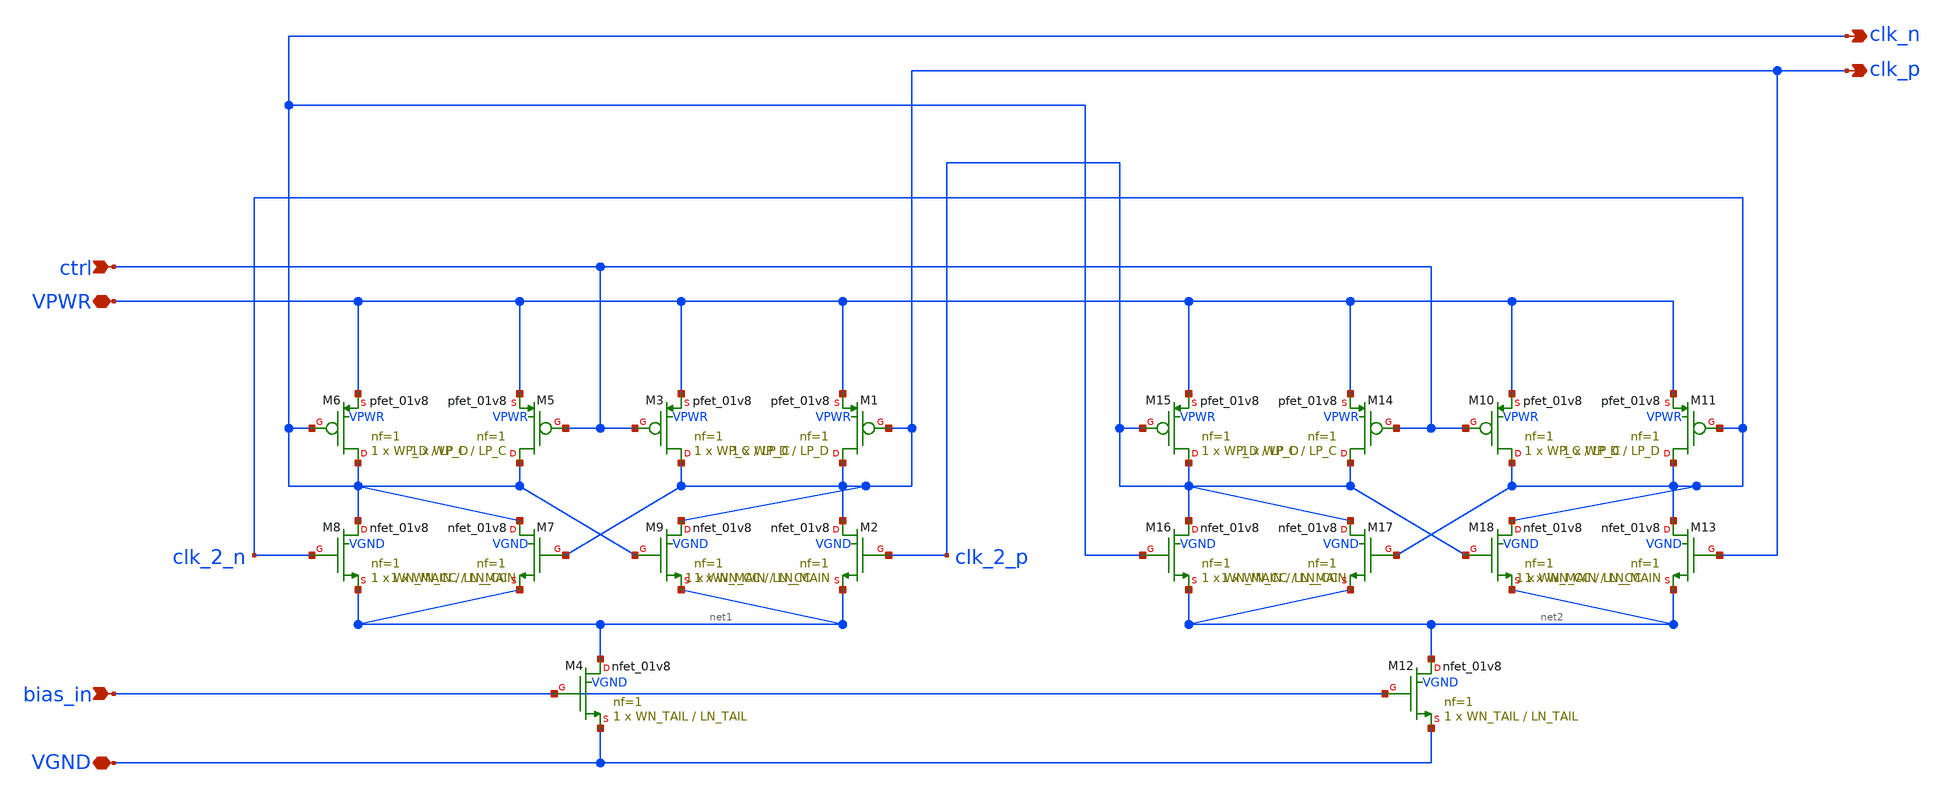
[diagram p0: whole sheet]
** sch_path: simple_vco/v1/clk_core.sch
**.subckt clk_core VPWR VGND ctrl bias_in clk_p clk_n
*.iopin VPWR
*.iopin VGND
*.ipin ctrl
*.ipin bias_in
*.opin clk_p
*.opin clk_n
XM3 clk_p ctrl VPWR VPWR sky130_fd_pr__pfet_01v8 L=LP_C W=WP_C nf=1 ad='int((1 + 1)/2) * WP_C / 1 * 0.29'
+ as='int((1 + 2)/2) * WP_C / 1 * 0.29' pd='2*int((1 + 1)/2) * (WP_C / 1 + 0.29)' ps='2*int((1 + 2)/2) * (WP_C / 1 + 0.29)'
+ nrd='0.29 / WP_C ' nrs='0.29 / WP_C ' sa=0 sb=0 sd=0 mult=1 m=1
XM1 clk_p clk_p VPWR VPWR sky130_fd_pr__pfet_01v8 L=LP_D W=WP_D nf=1 ad='int((1 + 1)/2) * WP_D / 1 * 0.29'
+ as='int((1 + 2)/2) * WP_D / 1 * 0.29' pd='2*int((1 + 1)/2) * (WP_D / 1 + 0.29)' ps='2*int((1 + 2)/2) * (WP_D / 1 + 0.29)'
+ nrd='0.29 / WP_D ' nrs='0.29 / WP_D ' sa=0 sb=0 sd=0 mult=1 m=1
XM4 net1 bias_in VGND VGND sky130_fd_pr__nfet_01v8 L=LN_TAIL W=WN_TAIL nf=1 ad='int((1 + 1)/2) * WN_TAIL / 1 * 0.29'
+ as='int((1 + 2)/2) * WN_TAIL / 1 * 0.29' pd='2*int((1 + 1)/2) * (WN_TAIL / 1 + 0.29)' ps='2*int((1 + 2)/2) * (WN_TAIL / 1 + 0.29)'
+ nrd='0.29 / WN_TAIL ' nrs='0.29 / WN_TAIL ' sa=0 sb=0 sd=0 mult=1 m=1
XM2 clk_p clk_2_p net1 VGND sky130_fd_pr__nfet_01v8 L=LN_MAIN W=WN_MAIN nf=1 ad='int((1 + 1)/2) * WN_MAIN / 1 * 0.29'
+ as='int((1 + 2)/2) * WN_MAIN / 1 * 0.29' pd='2*int((1 + 1)/2) * (WN_MAIN / 1 + 0.29)' ps='2*int((1 + 2)/2) * (WN_MAIN / 1 + 0.29)'
+ nrd='0.29 / WN_MAIN ' nrs='0.29 / WN_MAIN ' sa=0 sb=0 sd=0 mult=1 m=1
XM5 clk_n ctrl VPWR VPWR sky130_fd_pr__pfet_01v8 L=LP_C W=WP_C nf=1 ad='int((1 + 1)/2) * WP_C / 1 * 0.29'
+ as='int((1 + 2)/2) * WP_C / 1 * 0.29' pd='2*int((1 + 1)/2) * (WP_C / 1 + 0.29)' ps='2*int((1 + 2)/2) * (WP_C / 1 + 0.29)'
+ nrd='0.29 / WP_C ' nrs='0.29 / WP_C ' sa=0 sb=0 sd=0 mult=1 m=1
XM6 clk_n clk_n VPWR VPWR sky130_fd_pr__pfet_01v8 L=LP_D W=WP_D nf=1 ad='int((1 + 1)/2) * WP_D / 1 * 0.29'
+ as='int((1 + 2)/2) * WP_D / 1 * 0.29' pd='2*int((1 + 1)/2) * (WP_D / 1 + 0.29)' ps='2*int((1 + 2)/2) * (WP_D / 1 + 0.29)'
+ nrd='0.29 / WP_D ' nrs='0.29 / WP_D ' sa=0 sb=0 sd=0 mult=1 m=1
XM8 clk_n clk_2_n net1 VGND sky130_fd_pr__nfet_01v8 L=LN_MAIN W=WN_MAIN nf=1 ad='int((1 + 1)/2) * WN_MAIN / 1 * 0.29'
+ as='int((1 + 2)/2) * WN_MAIN / 1 * 0.29' pd='2*int((1 + 1)/2) * (WN_MAIN / 1 + 0.29)' ps='2*int((1 + 2)/2) * (WN_MAIN / 1 + 0.29)'
+ nrd='0.29 / WN_MAIN ' nrs='0.29 / WN_MAIN ' sa=0 sb=0 sd=0 mult=1 m=1
XM7 clk_n clk_p net1 VGND sky130_fd_pr__nfet_01v8 L=LN_CC W=WN_CC nf=1 ad='int((1 + 1)/2) * WN_CC / 1 * 0.29'
+ as='int((1 + 2)/2) * WN_CC / 1 * 0.29' pd='2*int((1 + 1)/2) * (WN_CC / 1 + 0.29)' ps='2*int((1 + 2)/2) * (WN_CC / 1 + 0.29)'
+ nrd='0.29 / WN_CC ' nrs='0.29 / WN_CC ' sa=0 sb=0 sd=0 mult=1 m=1
XM9 clk_p clk_n net1 VGND sky130_fd_pr__nfet_01v8 L=LN_CC W=WN_CC nf=1 ad='int((1 + 1)/2) * WN_CC / 1 * 0.29'
+ as='int((1 + 2)/2) * WN_CC / 1 * 0.29' pd='2*int((1 + 1)/2) * (WN_CC / 1 + 0.29)' ps='2*int((1 + 2)/2) * (WN_CC / 1 + 0.29)'
+ nrd='0.29 / WN_CC ' nrs='0.29 / WN_CC ' sa=0 sb=0 sd=0 mult=1 m=1
XM10 clk_2_n ctrl VPWR VPWR sky130_fd_pr__pfet_01v8 L=LP_C W=WP_C nf=1 ad='int((1 + 1)/2) * WP_C / 1 * 0.29'
+ as='int((1 + 2)/2) * WP_C / 1 * 0.29' pd='2*int((1 + 1)/2) * (WP_C / 1 + 0.29)' ps='2*int((1 + 2)/2) * (WP_C / 1 + 0.29)'
+ nrd='0.29 / WP_C ' nrs='0.29 / WP_C ' sa=0 sb=0 sd=0 mult=1 m=1
XM11 clk_2_n clk_2_n VPWR VPWR sky130_fd_pr__pfet_01v8 L=LP_D W=WP_D nf=1 ad='int((1 + 1)/2) * WP_D / 1 * 0.29'
+ as='int((1 + 2)/2) * WP_D / 1 * 0.29' pd='2*int((1 + 1)/2) * (WP_D / 1 + 0.29)' ps='2*int((1 + 2)/2) * (WP_D / 1 + 0.29)'
+ nrd='0.29 / WP_D ' nrs='0.29 / WP_D ' sa=0 sb=0 sd=0 mult=1 m=1
XM12 net2 bias_in VGND VGND sky130_fd_pr__nfet_01v8 L=LN_TAIL W=WN_TAIL nf=1 ad='int((1 + 1)/2) * WN_TAIL / 1 * 0.29'
+ as='int((1 + 2)/2) * WN_TAIL / 1 * 0.29' pd='2*int((1 + 1)/2) * (WN_TAIL / 1 + 0.29)' ps='2*int((1 + 2)/2) * (WN_TAIL / 1 + 0.29)'
+ nrd='0.29 / WN_TAIL ' nrs='0.29 / WN_TAIL ' sa=0 sb=0 sd=0 mult=1 m=1
XM13 clk_2_n clk_p net2 VGND sky130_fd_pr__nfet_01v8 L=LN_MAIN W=WN_MAIN nf=1 ad='int((1 + 1)/2) * WN_MAIN / 1 * 0.29'
+ as='int((1 + 2)/2) * WN_MAIN / 1 * 0.29' pd='2*int((1 + 1)/2) * (WN_MAIN / 1 + 0.29)' ps='2*int((1 + 2)/2) * (WN_MAIN / 1 + 0.29)'
+ nrd='0.29 / WN_MAIN ' nrs='0.29 / WN_MAIN ' sa=0 sb=0 sd=0 mult=1 m=1
XM14 clk_2_p ctrl VPWR VPWR sky130_fd_pr__pfet_01v8 L=LP_C W=WP_C nf=1 ad='int((1 + 1)/2) * WP_C / 1 * 0.29'
+ as='int((1 + 2)/2) * WP_C / 1 * 0.29' pd='2*int((1 + 1)/2) * (WP_C / 1 + 0.29)' ps='2*int((1 + 2)/2) * (WP_C / 1 + 0.29)'
+ nrd='0.29 / WP_C ' nrs='0.29 / WP_C ' sa=0 sb=0 sd=0 mult=1 m=1
XM15 clk_2_p clk_2_p VPWR VPWR sky130_fd_pr__pfet_01v8 L=LP_D W=WP_D nf=1 ad='int((1 + 1)/2) * WP_D / 1 * 0.29'
+ as='int((1 + 2)/2) * WP_D / 1 * 0.29' pd='2*int((1 + 1)/2) * (WP_D / 1 + 0.29)' ps='2*int((1 + 2)/2) * (WP_D / 1 + 0.29)'
+ nrd='0.29 / WP_D ' nrs='0.29 / WP_D ' sa=0 sb=0 sd=0 mult=1 m=1
XM16 clk_2_p clk_n net2 VGND sky130_fd_pr__nfet_01v8 L=LN_MAIN W=WN_MAIN nf=1 ad='int((1 + 1)/2) * WN_MAIN / 1 * 0.29'
+ as='int((1 + 2)/2) * WN_MAIN / 1 * 0.29' pd='2*int((1 + 1)/2) * (WN_MAIN / 1 + 0.29)' ps='2*int((1 + 2)/2) * (WN_MAIN / 1 + 0.29)'
+ nrd='0.29 / WN_MAIN ' nrs='0.29 / WN_MAIN ' sa=0 sb=0 sd=0 mult=1 m=1
XM17 clk_2_p clk_2_n net2 VGND sky130_fd_pr__nfet_01v8 L=LN_CC W=WN_CC nf=1 ad='int((1 + 1)/2) * WN_CC / 1 * 0.29'
+ as='int((1 + 2)/2) * WN_CC / 1 * 0.29' pd='2*int((1 + 1)/2) * (WN_CC / 1 + 0.29)' ps='2*int((1 + 2)/2) * (WN_CC / 1 + 0.29)'
+ nrd='0.29 / WN_CC ' nrs='0.29 / WN_CC ' sa=0 sb=0 sd=0 mult=1 m=1
XM18 clk_2_n clk_2_p net2 VGND sky130_fd_pr__nfet_01v8 L=LN_CC W=WN_CC nf=1 ad='int((1 + 1)/2) * WN_CC / 1 * 0.29'
+ as='int((1 + 2)/2) * WN_CC / 1 * 0.29' pd='2*int((1 + 1)/2) * (WN_CC / 1 + 0.29)' ps='2*int((1 + 2)/2) * (WN_CC / 1 + 0.29)'
+ nrd='0.29 / WN_CC ' nrs='0.29 / WN_CC ' sa=0 sb=0 sd=0 mult=1 m=1
**.ends
.end
